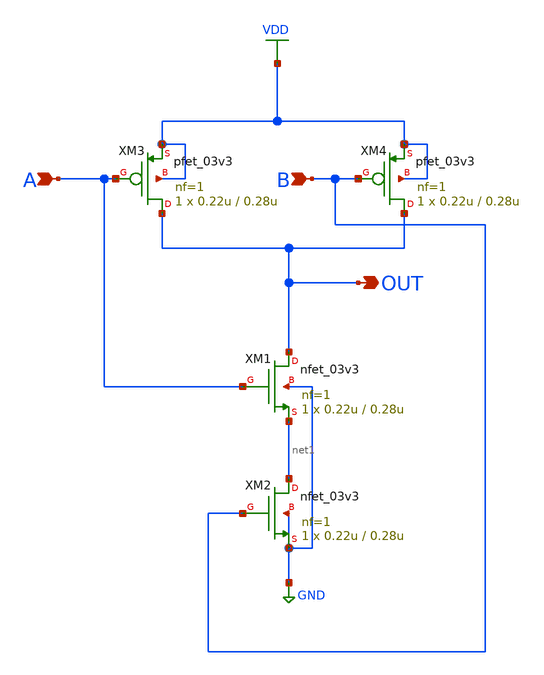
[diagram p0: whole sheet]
** sch_path: designs/schematics/mux2x1/nand.sch
**.subckt nand B A OUT
*.ipin B
*.ipin A
*.opin OUT
XM1 OUT A net1 GND nfet_03v3 L=0.28u W=0.22u nf=1 ad='int((nf+1)/2) * W/nf * 0.18u' as='int((nf+2)/2) * W/nf * 0.18u'
+ pd='2*int((nf+1)/2) * (W/nf + 0.18u)' ps='2*int((nf+2)/2) * (W/nf + 0.18u)' nrd='0.18u / W' nrs='0.18u / W'
+ sa=0 sb=0 sd=0 m=1
XM2 net1 B GND GND nfet_03v3 L=0.28u W=0.22u nf=1 ad='int((nf+1)/2) * W/nf * 0.18u' as='int((nf+2)/2) * W/nf * 0.18u'
+ pd='2*int((nf+1)/2) * (W/nf + 0.18u)' ps='2*int((nf+2)/2) * (W/nf + 0.18u)' nrd='0.18u / W' nrs='0.18u / W'
+ sa=0 sb=0 sd=0 m=1
XM3 OUT A VDD VDD pfet_03v3 L=0.28u W=0.22u nf=1 ad='int((nf+1)/2) * W/nf * 0.18u' as='int((nf+2)/2) * W/nf * 0.18u'
+ pd='2*int((nf+1)/2) * (W/nf + 0.18u)' ps='2*int((nf+2)/2) * (W/nf + 0.18u)' nrd='0.18u / W' nrs='0.18u / W'
+ sa=0 sb=0 sd=0 m=1
XM4 OUT B VDD VDD pfet_03v3 L=0.28u W=0.22u nf=1 ad='int((nf+1)/2) * W/nf * 0.18u' as='int((nf+2)/2) * W/nf * 0.18u'
+ pd='2*int((nf+1)/2) * (W/nf + 0.18u)' ps='2*int((nf+2)/2) * (W/nf + 0.18u)' nrd='0.18u / W' nrs='0.18u / W'
+ sa=0 sb=0 sd=0 m=1
**.ends
.GLOBAL VDD
.GLOBAL GND
.end
